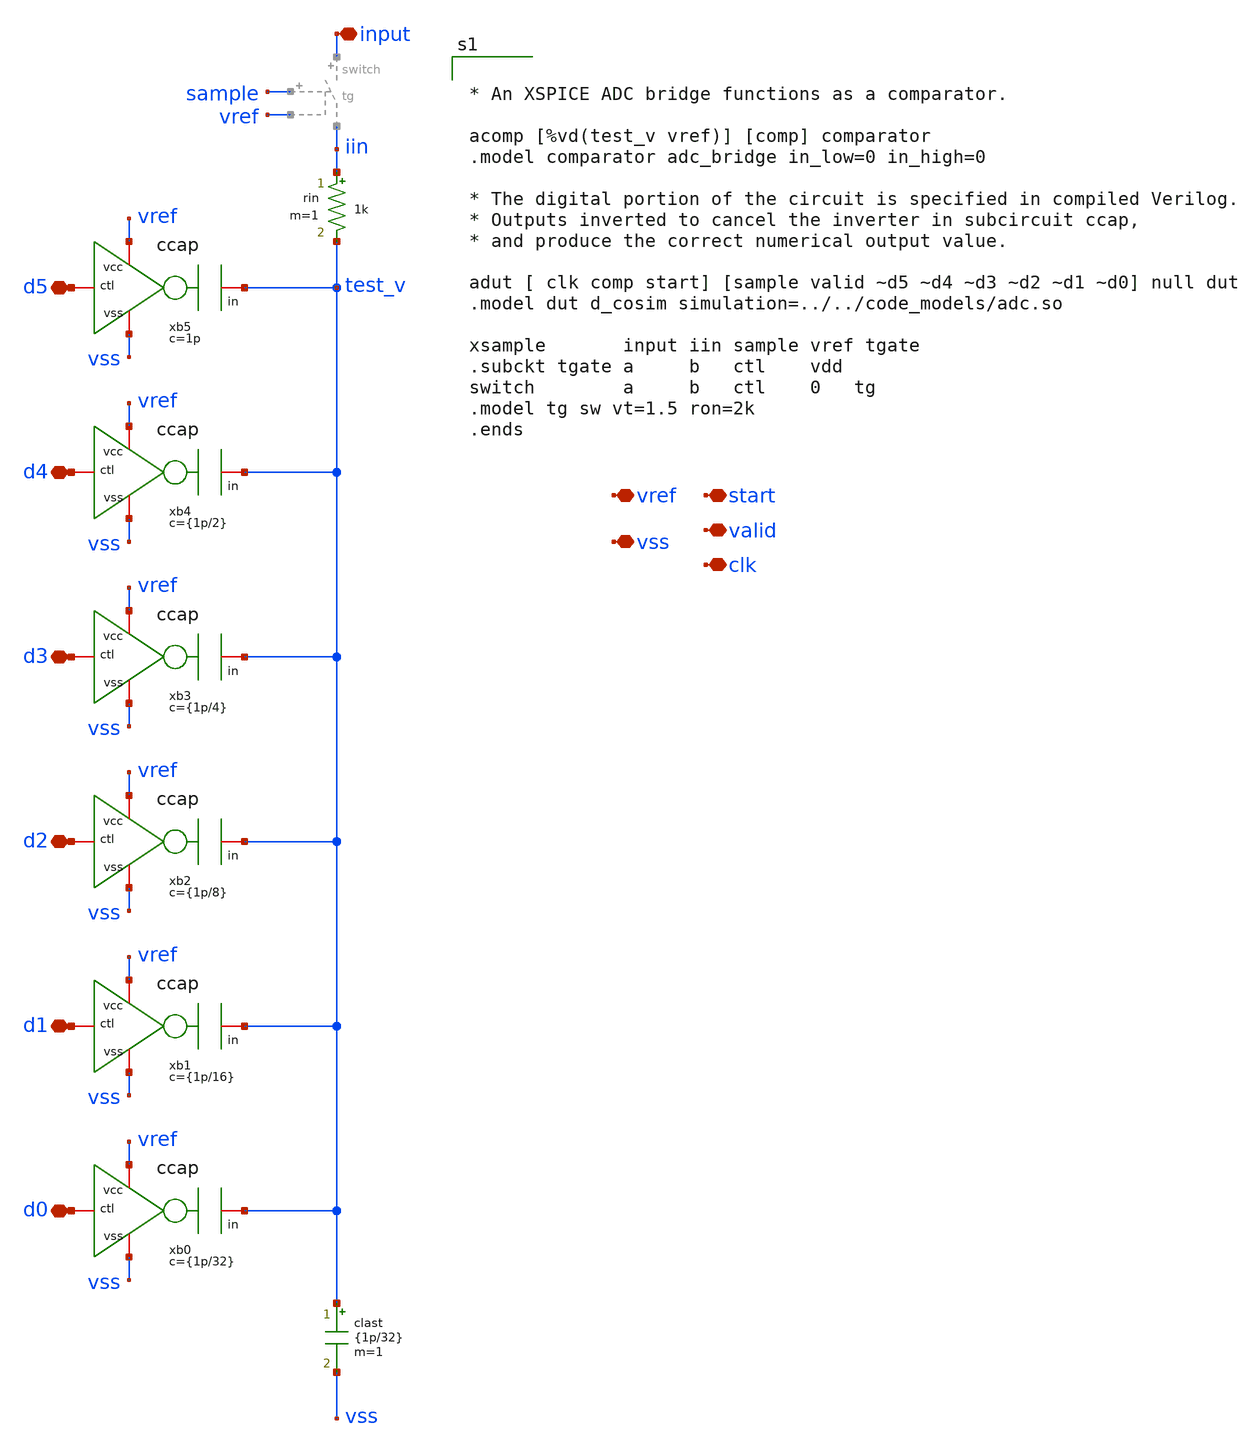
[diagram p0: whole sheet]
** sch_path: samples/digital_cosimulation/adc/symbol/adc.sch
**.subckt adc vss vref start valid d5 d4 d3 d2 d1 clk d0 input
*.iopin vss
*.iopin vref
*.iopin start
*.iopin valid
*.iopin d5
*.iopin d4
*.iopin d3
*.iopin d2
*.iopin d1
*.iopin clk
*.iopin d0
*.iopin input
rin iin test_v 1k m=1
xb5 test_v vref d5 vss ccap c=1p
xb4 test_v vref d4 vss ccap c={1p/2}
xb3 test_v vref d3 vss ccap c={1p/4}
xb2 test_v vref d2 vss ccap c={1p/8}
xb1 test_v vref d1 vss ccap c={1p/16}
xb0 test_v vref d0 vss ccap c={1p/32}
clast test_v vss {1p/32} m=1
**** begin user architecture code


* An XSPICE ADC bridge functions as a comparator.

acomp [%vd(test_v vref)] [comp] comparator
.model comparator adc_bridge in_low=0 in_high=0

* The digital portion of the circuit is specified in compiled Verilog.
* Outputs inverted to cancel the inverter in subcircuit ccap,
* and produce the correct numerical output value.

adut [ clk comp start] [sample valid ~d5 ~d4 ~d3 ~d2 ~d1 ~d0] null dut
.model dut d_cosim simulation=../../code_models/adc.so

xsample       input iin sample vref tgate
.subckt tgate a     b   ctl    vdd
switch        a     b   ctl    0   tg
.model tg sw vt=1.5 ron=2k
.ends


**** end user architecture code
**.ends

* expanding   symbol:  symbol/ccap.sym # of pins=4
** sym_path: samples/digital_cosimulation/ccap/symbol/ccap.sym
** sch_path: samples/digital_cosimulation/ccap/symbol/ccap.sch
.subckt ccap in vcc ctl vss  c=1p
*.iopin ctl
*.iopin in
*.iopin vcc
*.iopin vss
xinv ctl tail vcc vss ainv
cb in tail {c} m=1
.ends


* expanding   symbol:  symbol/ainv.sym # of pins=4
** sym_path: samples/digital_cosimulation/ainv/symbol/ainv.sym
** sch_path: samples/digital_cosimulation/ainv/symbol/ainv.sch
.subckt ainv in out vdd vss
*.iopin vdd
*.iopin out
*.iopin vss
*.iopin in
**** begin user architecture code


.model p1 pmos   level=2 vto=-0.5 kp=8.5e-6 gamma=0.4 phi=0.65 lambda=0.05 xj=0.5e-6
.model n1 nmos   level=2 vto=0.5 kp=24e-6 gamma=0.15 phi=0.65 lambda=0.015 xj=0.5e-6


**** end user architecture code
mn out in vss vss n1 w=5u l=0.18u m=1
mp out in vdd vdd p1 w=5u l=0.18u m=1
.ends

.end
